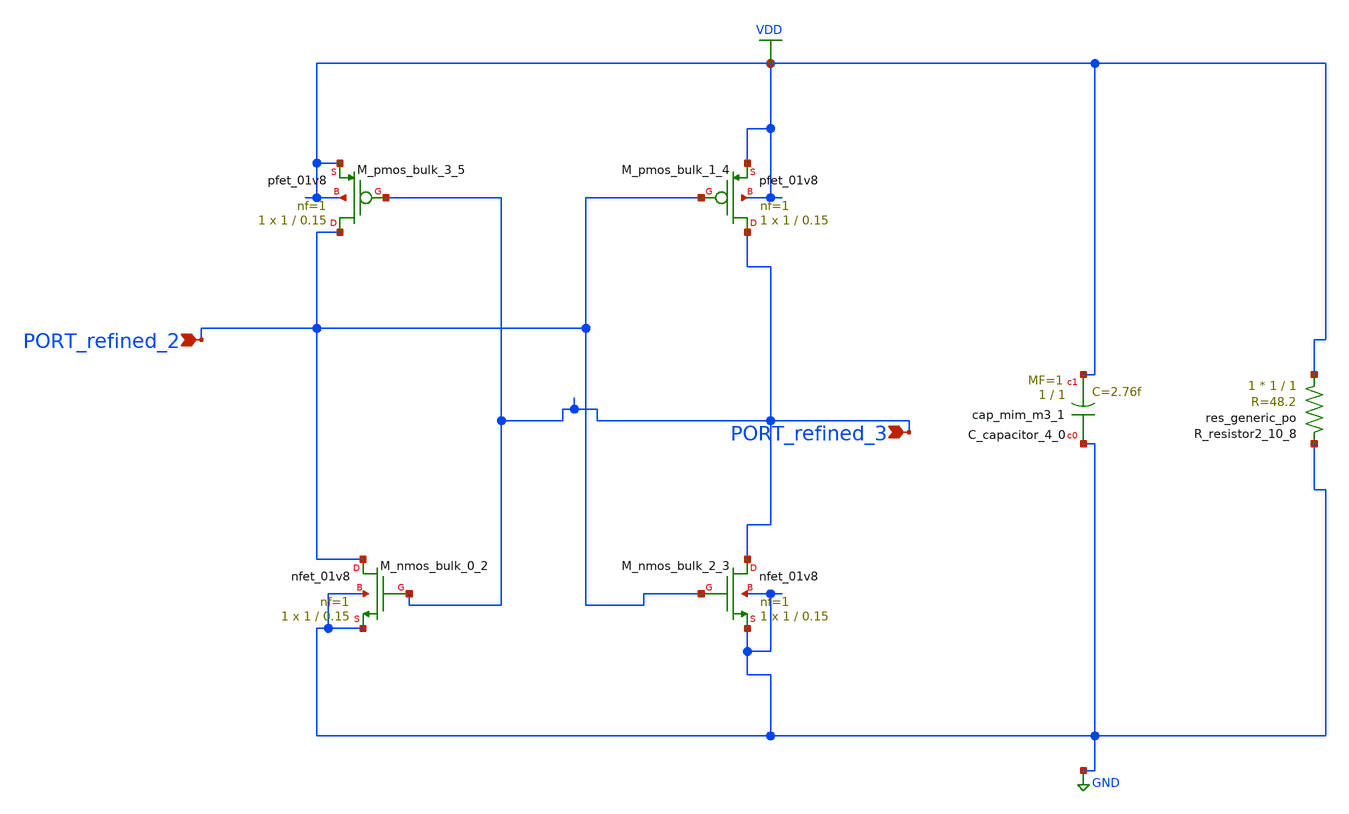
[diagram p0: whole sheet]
** sch_path: schematics/10_1007_s10470-023-02166-8_05_001_crop1.sch
**.subckt 10_1007_s10470-023-02166-8_05_001_crop1 PORT_refined_2 PORT_refined_3
*.ipin PORT_refined_2
*.ipin PORT_refined_3
XC_capacitor_4_0 GND VDD sky130_fd_pr__cap_mim_m3_1 W=1 L=1 MF=1 m=1
XM_nmos_bulk_0_2 PORT_refined_2 PORT_refined_3 GND GND sky130_fd_pr__nfet_01v8 L=0.15 W=1 nf=1 ad='int((1 + 1)/2) * 1 / 1 * 0.29'
+ as='int((1 + 2)/2) * 1 / 1 * 0.29' pd='2*int((1 + 1)/2) * (1 / 1 + 0.29)' ps='2*int((1 + 2)/2) * (1 / 1 + 0.29)'
+ nrd='0.29 / 1 ' nrs='0.29 / 1 ' sa=0 sb=0 sd=0 mult=1 m=1
XM_nmos_bulk_2_3 PORT_refined_3 PORT_refined_2 GND GND sky130_fd_pr__nfet_01v8 L=0.15 W=1 nf=1 ad='int((1 + 1)/2) * 1 / 1 * 0.29'
+ as='int((1 + 2)/2) * 1 / 1 * 0.29' pd='2*int((1 + 1)/2) * (1 / 1 + 0.29)' ps='2*int((1 + 2)/2) * (1 / 1 + 0.29)'
+ nrd='0.29 / 1 ' nrs='0.29 / 1 ' sa=0 sb=0 sd=0 mult=1 m=1
XM_pmos_bulk_1_4 PORT_refined_3 PORT_refined_2 VDD VDD sky130_fd_pr__pfet_01v8 L=0.15 W=1 nf=1 ad='int((1 + 1)/2) * 1 / 1 * 0.29'
+ as='int((1 + 2)/2) * 1 / 1 * 0.29' pd='2*int((1 + 1)/2) * (1 / 1 + 0.29)' ps='2*int((1 + 2)/2) * (1 / 1 + 0.29)'
+ nrd='0.29 / 1 ' nrs='0.29 / 1 ' sa=0 sb=0 sd=0 mult=1 m=1
XM_pmos_bulk_3_5 PORT_refined_2 PORT_refined_3 VDD VDD sky130_fd_pr__pfet_01v8 L=0.15 W=1 nf=1 ad='int((1 + 1)/2) * 1 / 1 * 0.29'
+ as='int((1 + 2)/2) * 1 / 1 * 0.29' pd='2*int((1 + 1)/2) * (1 / 1 + 0.29)' ps='2*int((1 + 2)/2) * (1 / 1 + 0.29)'
+ nrd='0.29 / 1 ' nrs='0.29 / 1 ' sa=0 sb=0 sd=0 mult=1 m=1
XR_resistor2_10_8 VDD GND sky130_fd_pr__res_generic_po W=1 L=1 m=1
**.ends
.GLOBAL GND
.GLOBAL VDD
.end
